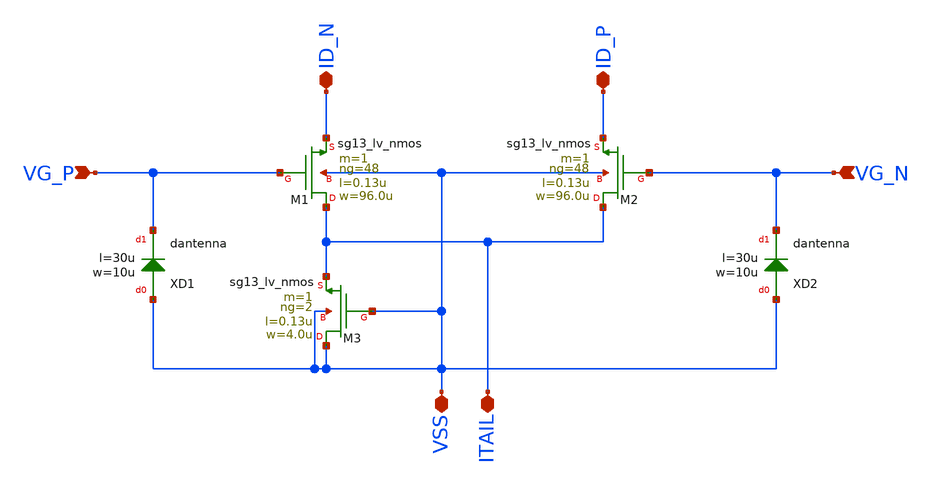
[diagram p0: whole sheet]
** sch_path: JKU_TC1/design_data/sfl-test-cells/xschem/diffpairs/dp_n_100u_130n.sch
**.subckt dp_n_100u_130n VG_P VG_N VSS ITAIL ID_N ID_P
*.ipin VG_P
*.ipin VG_N
*.iopin VSS
*.iopin ITAIL
*.iopin ID_N
*.iopin ID_P
XM1 ITAIL VG_P ID_N VSS sg13_lv_nmos w=96.0u l=0.13u ng=48 m=1 mm_ok=1
XM2 ITAIL VG_N ID_P VSS sg13_lv_nmos w=96.0u l=0.13u ng=48 m=1 mm_ok=1
XM3 VSS VSS ITAIL VSS sg13_lv_nmos w=4.0u l=0.13u ng=2 m=1 mm_ok=1
XXD1 VSS VG_P dantenna l=30u w=10u
XXD2 VSS VG_N dantenna l=30u w=10u
**.ends
.end
